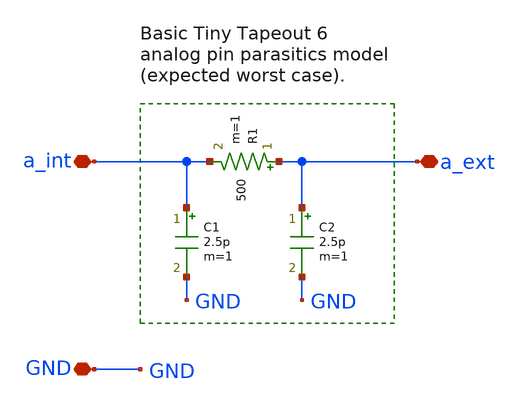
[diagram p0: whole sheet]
** sch_path: xschem/tt06_analog_load.sch
**.subckt tt06_analog_load a_int a_ext GND
*.iopin a_int
*.iopin a_ext
*.iopin GND
R1 a_ext a_int 500 m=1
C1 a_int GND 2.5p m=1
C2 a_ext GND 2.5p m=1
**.ends
.end
